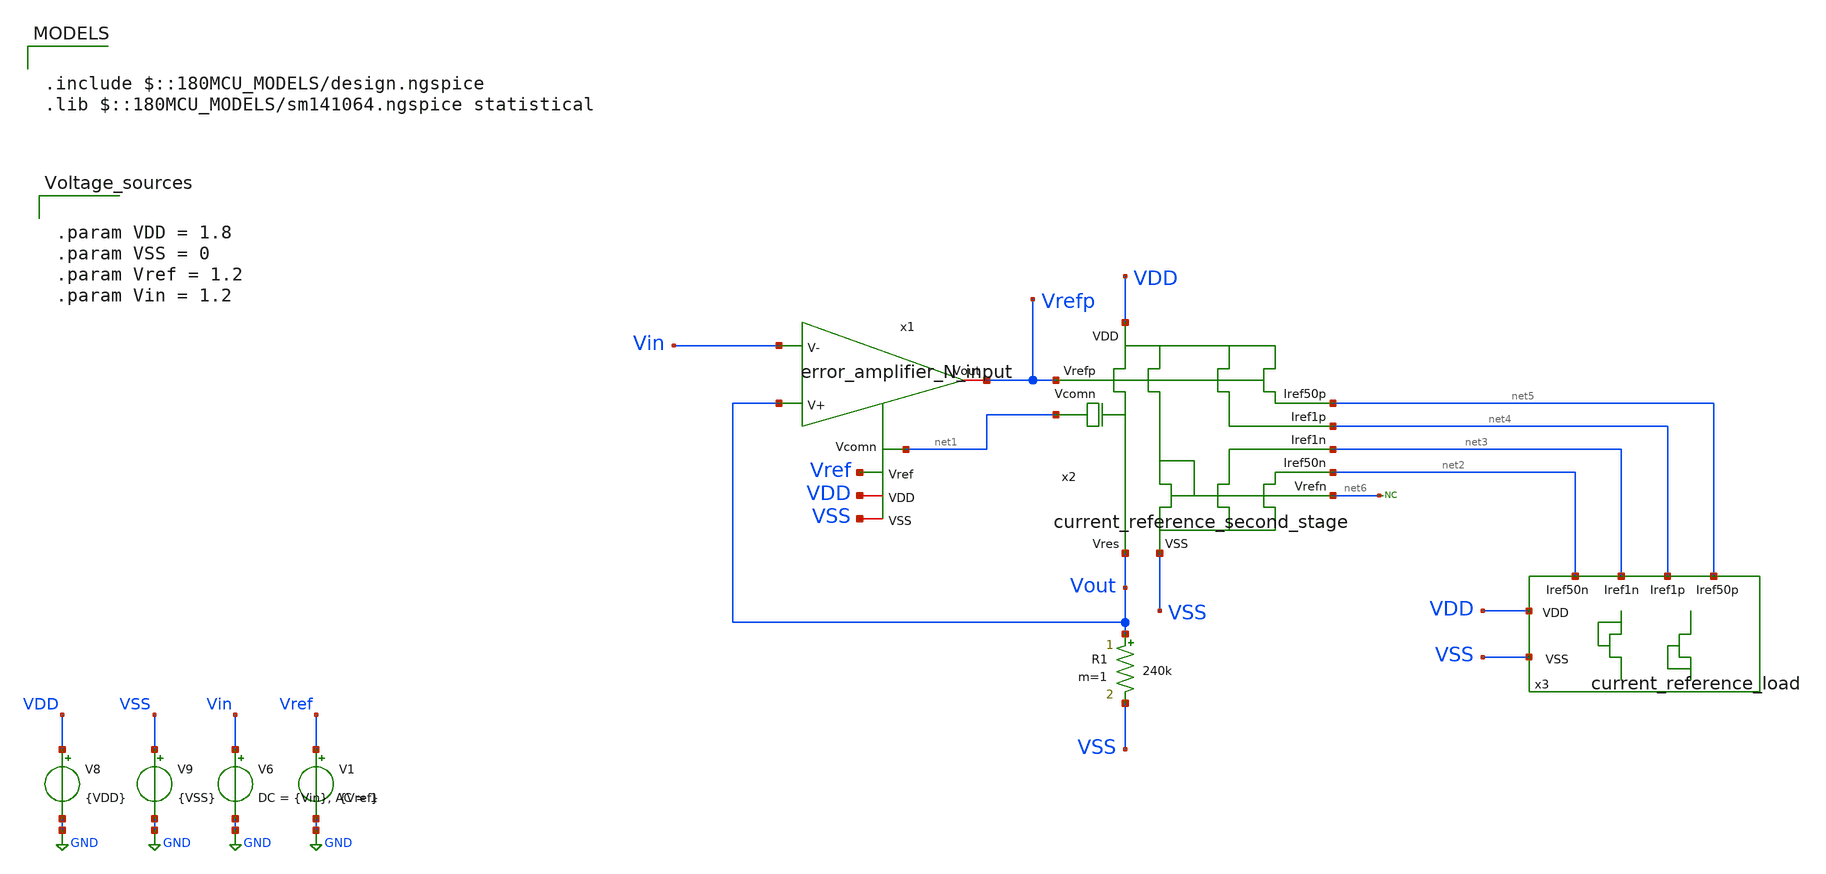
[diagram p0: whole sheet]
** sch_path: designs/current_reference_generator/xschem/current_reference_generator_TB_mc.sch
**.subckt current_reference_generator_TB_mc
R1 Vout VSS 240k m=1
* noconn #net6
x2 net1 Vout VSS VDD Vrefp net6 net3 net2 net4 net5 current_reference_second_stage
x3 net3 net2 net4 net5 VDD VSS current_reference_load
x1 Vrefp Vout Vin Vref VDD VSS net1 error_amplifier_N_input
V6 Vin GND DC = {Vin}, AC = 1
V8 VDD GND {VDD}
V9 VSS GND {VSS}
V1 Vref GND {Vref}
**** begin user architecture code

.include $::180MCU_MODELS/design.ngspice
.lib $::180MCU_MODELS/sm141064.ngspice statistical



.param VDD = 1.8
.param VSS = 0
.param Vref = 1.2
.param Vin = 1.2






*.param TEMPGAUSS = agauss(40, 30, 1)
*.option temp = 'TEMPGAUSS'

.save @m.x3.xm1.m0[id]
.save @m.x3.xm2.m0[id]
.save @m.x3.xm3.m0[id]
.save @m.x3.xm4.m0[id]
.param sw_stat_global = 1
.param sw_stat_mismatch = 1

*.save all
.control
  let mc_runs = 1000
  let run = 0
  set curplot=new          $ create a new plot
  set scratch=$curplot     $ store its name to 'scratch'
  setplot $scratch         $ make 'scratch' the active plot
  let current_n1=unitvec(mc_runs) $ create a vector in plot 'scratch' to store current_n1 data
  let current_n50=unitvec(mc_runs) $ create a vector in plot 'scratch' to store current_n50 data
  let current_p1=unitvec(mc_runs) $ create a vector in plot 'scratch' to store current_p1 data
  let current_p50=unitvec(mc_runs) $ create a vector in plot 'scratch' to store current_p50 data

  dowhile run < mc_runs

    *MC statistical

    op

    let id_n1 = @m.x3.xm1.m0[id]
    let id_n50 = @m.x3.xm2.m0[id]
    let id_p1 = @m.x3.xm3.m0[id]
    let id_p50 = @m.x3.xm4.m0[id]

    print id_n1 id_n50 id_p1 id_p50

    set run = $&run             $ create a variable from the vector
    set dt = $curplot           $ store the current plot to dt
    setplot $scratch            $ make 'scratch' the active plot

    let current_n1[run]={$dt}.id_n1       $ store In to vector Current in plot 'scratch'
    let current_n50[run]={$dt}.id_n50       $ store In to vector Current in plot 'scratch'
    let current_p1[run]={$dt}.id_p1       $ store In to vector Current in plot 'scratch'
    let current_p50[run]={$dt}.id_p50       $ store In to vector Current in plot 'scratch'

    setplot $dt                 $ go back to the previous plot

    let run = run + 1
    reset
  end    $ loop ends here

  echo
  *print {$scratch}.current_n1
  *print {$scratch}.current_n50
  *print {$scratch}.current_p1
  *print {$scratch}.current_p50

* Compute statistics

let mean_val_n1 = avg({$scratch}.current_n1)          ; Store mean in scalar variable
let mean_n1 = mean_val_n1[mc_runs-1]
let diff_n1 = {$scratch}.current_n1 - mean_val_n1
let diff_sq_n1 = diff_n1 * diff_n1
let variance_n1 = avg(diff_sq_n1)
let stddev_val_n1 = sqrt(variance_n1)  ; Store stddev in scalar variable
let stddev_n1 = stddev_val_n1[mc_runs-1]

let mean_val_n50 = avg({$scratch}.current_n50)          ; Store mean in scalar variable
let mean_n50 = mean_val_n50[mc_runs-1]
let diff_n50 = {$scratch}.current_n50 - mean_val_n50
let diff_sq_n50 = diff_n50 * diff_n50
let variance_n50 = avg(diff_sq_n50)
let stddev_val_n50 = sqrt(variance_n50)  ; Store stddev in scalar variable
let stddev_n50 = stddev_val_n50[mc_runs-1]

let mean_val_p1 = avg({$scratch}.current_p1)          ; Store mean in scalar variable
let mean_p1 = mean_val_p1[mc_runs-1]
let diff_p1 = {$scratch}.current_p1 - mean_val_p1
let diff_sq_p1 = diff_p1 * diff_p1
let variance_p1 = avg(diff_sq_p1)
let stddev_val_p1 = sqrt(variance_p1)  ; Store stddev in scalar variable
let stddev_p1 = stddev_val_p1[mc_runs-1]

let mean_val_p50 = avg({$scratch}.current_p50)          ; Store mean in scalar variable
let mean_p50 = mean_val_p50[mc_runs-1]
let diff_p50 = {$scratch}.current_p50 - mean_val_p50
let diff_sq_p50 = diff_p50 * diff_p50
let variance_p50 = avg(diff_sq_p50)
let stddev_val_p50 = sqrt(variance_p50)  ; Store stddev in scalar variable
let stddev_p50 = stddev_val_p50[mc_runs-1]

* Print statistics
echo
echo '----------------------------------------'
echo 'Monte Carlo Results (n = $&mc_runs)'
echo '----------------------------------------'
echo 'Mean Id_n1: $&mean_n1 A'
echo 'Std Dev Id_n1: $&stddev_n1 A'
echo '----------------------------------------'
echo 'Mean Id_n50: $&mean_n50 A'
echo 'Std Dev Id_n50: $&stddev_n50 A'
echo '----------------------------------------'
echo 'Mean Id_p1: $&mean_p1 A'
echo 'Std Dev Id_p1: $&stddev_p1 A'
echo '----------------------------------------'
echo 'Mean Id_p50: $&mean_p50 A'
echo 'Std Dev Id_p50: $&stddev_p50 A'
echo '----------------------------------------'


.endc



**** end user architecture code
**.ends
.GLOBAL GND
.end
